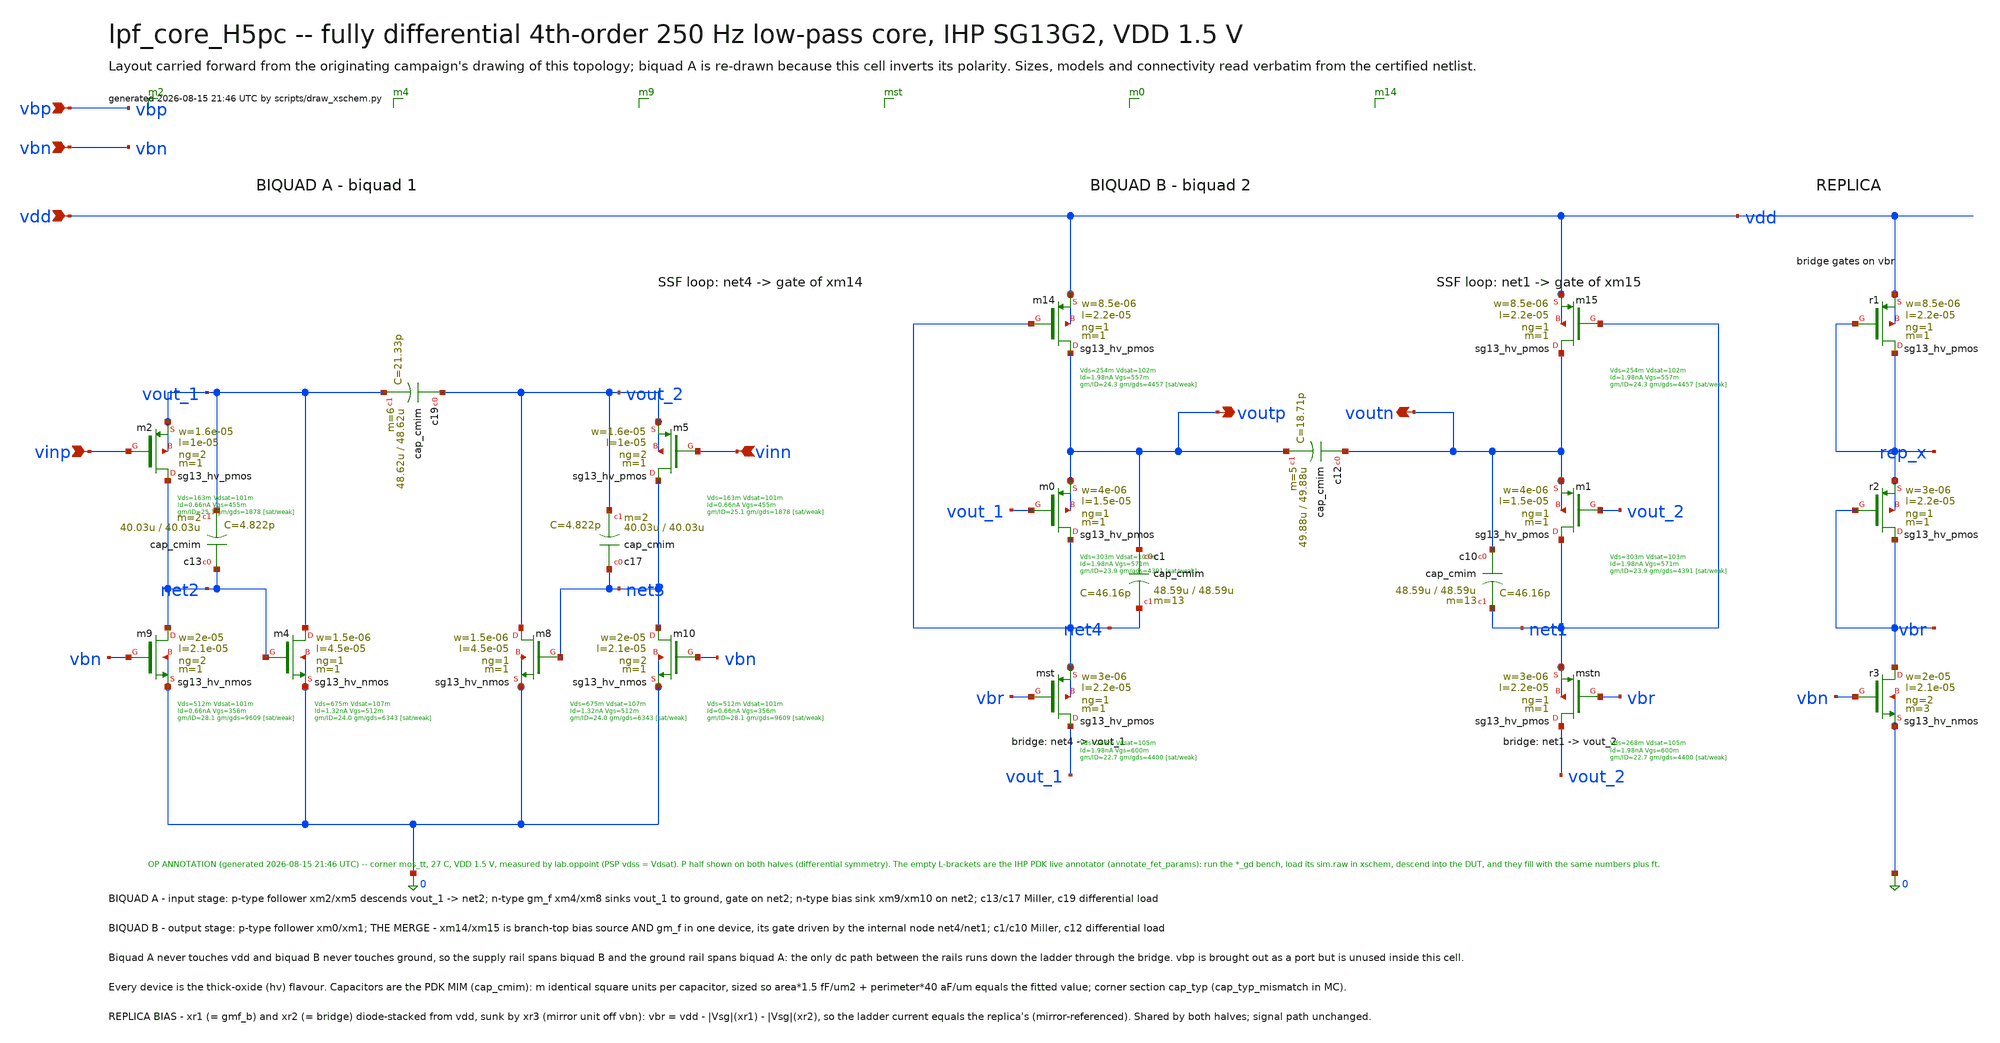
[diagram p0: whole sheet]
** sch_path: signoff/post-pvt/H5-pdk-cap/lpf_core_H5pc.sch
**.subckt lpf_core_H5pc vinp vinn voutp voutn vdd vbn vbp
*.ipin vinp
*.ipin vinn
*.opin voutp
*.opin voutn
*.ipin vdd
*.ipin vbn
*.ipin vbp
Xm2 net2 vinp vout_1 vout_1 sg13_hv_pmos w=1.6e-05 l=1e-05 ng=2 m=1 mm_ok=1
Xm5 net3 vinn vout_2 vout_2 sg13_hv_pmos w=1.6e-05 l=1e-05 ng=2 m=1 mm_ok=1
Xm4 vout_1 net2 0 0 sg13_hv_nmos w=1.5e-06 l=4.5e-05 ng=1 m=1 mm_ok=1
Xm8 vout_2 net3 0 0 sg13_hv_nmos w=1.5e-06 l=4.5e-05 ng=1 m=1 mm_ok=1
Xm9 net2 vbn 0 0 sg13_hv_nmos w=2e-05 l=2.1e-05 ng=2 m=1 mm_ok=1
Xm10 net3 vbn 0 0 sg13_hv_nmos w=2e-05 l=2.1e-05 ng=2 m=1 mm_ok=1
Xmst vout_1 vbr net4 net4 sg13_hv_pmos w=3e-06 l=2.2e-05 ng=1 m=1 mm_ok=1
Xmstn vout_2 vbr net1 net1 sg13_hv_pmos w=3e-06 l=2.2e-05 ng=1 m=1 mm_ok=1
Xm0 net4 vout_1 voutp voutp sg13_hv_pmos w=4e-06 l=1.5e-05 ng=1 m=1 mm_ok=1
Xm1 net1 vout_2 voutn voutn sg13_hv_pmos w=4e-06 l=1.5e-05 ng=1 m=1 mm_ok=1
Xm14 voutp net4 vdd vdd sg13_hv_pmos w=8.5e-06 l=2.2e-05 ng=1 m=1 mm_ok=1
Xm15 voutn net1 vdd vdd sg13_hv_pmos w=8.5e-06 l=2.2e-05 ng=1 m=1 mm_ok=1
Xr1 rep_x rep_x vdd vdd sg13_hv_pmos w=8.5e-06 l=2.2e-05 ng=1 m=1 mm_ok=1
Xr2 vbr vbr rep_x rep_x sg13_hv_pmos w=3e-06 l=2.2e-05 ng=1 m=1 mm_ok=1
Xr3 vbr vbn 0 0 sg13_hv_nmos w=2e-05 l=2.1e-05 ng=2 m=3 mm_ok=1
Xc13 net2 vout_1 cap_cmim w=40.03u l=40.03u m=2 mm_ok=1
Xc17 net3 vout_2 cap_cmim w=40.03u l=40.03u m=2 mm_ok=1
Xc19 vout_2 vout_1 cap_cmim w=48.62u l=48.62u m=6 mm_ok=1
Xc1 voutp net4 cap_cmim w=48.59u l=48.59u m=13 mm_ok=1
Xc10 voutn net1 cap_cmim w=48.59u l=48.59u m=13 mm_ok=1
Xc12 voutn voutp cap_cmim w=49.88u l=49.88u m=5 mm_ok=1
**.ends
.end
